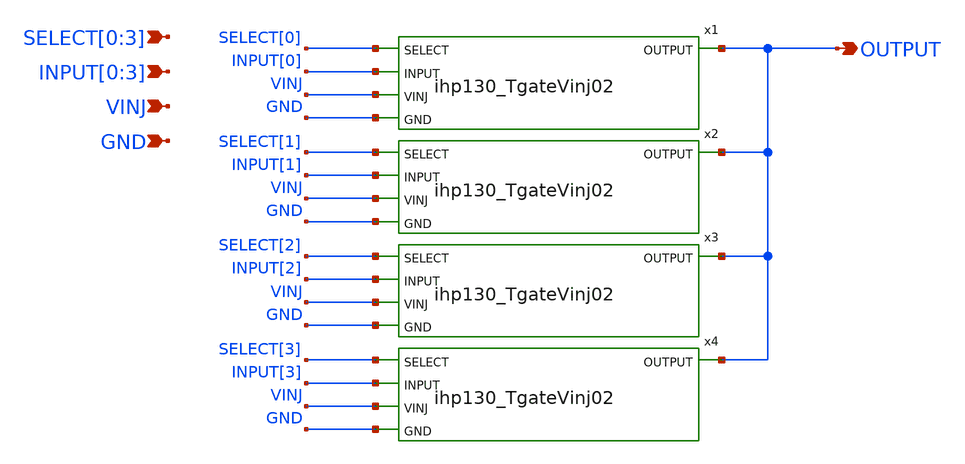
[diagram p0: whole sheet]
** sch_path: ihp130_cells/4TgateVinj/4TgateVinj.sch
**.subckt 4TgateVinj SELECT[0],SELECT[1],SELECT[2],SELECT[3] INPUT[0],INPUT[1],INPUT[2],INPUT[3]
*+ VINJ GND OUTPUT
*.ipin SELECT[0],SELECT[1],SELECT[2],SELECT[3]
*.ipin INPUT[0],INPUT[1],INPUT[2],INPUT[3]
*.ipin VINJ
*.ipin GND
*.opin OUTPUT
x1 SELECT[0] INPUT[0] VINJ GND OUTPUT ihp130_TgateVinj02
x2 SELECT[1] INPUT[1] VINJ GND OUTPUT ihp130_TgateVinj02
x3 SELECT[2] INPUT[2] VINJ GND OUTPUT ihp130_TgateVinj02
x4 SELECT[3] INPUT[3] VINJ GND OUTPUT ihp130_TgateVinj02
**.ends

* expanding   symbol:  TgateVinj02/ihp130_TgateVinj02.sym # of pins=5
** sym_path: ihp130_cells/TgateVinj02/ihp130_TgateVinj02.sym
** sch_path: ihp130_cells/TgateVinj02/ihp130_TgateVinj02.sch
.subckt ihp130_TgateVinj02 SELECT INPUT VINJ GND OUTPUT
*.ipin SELECT
*.ipin INPUT
*.ipin VINJ
*.ipin GND
*.opin OUTPUT
XM1 Selb SELECT VINJ VINJ sg13_hv_pmos w=0.42u l=0.5u ng=1 m=1 mm_ok=1
XM2 Selb SELECT GND GND sg13_hv_nmos w=0.42u l=0.5u ng=1 m=1 mm_ok=1
XM3 INPUT Selb OUTPUT VINJ sg13_hv_pmos w=0.42u l=0.5u ng=1 m=1 mm_ok=1
XM4 INPUT SELECT OUTPUT GND sg13_hv_nmos w=0.42u l=0.5u ng=1 m=1 mm_ok=1
.ends

.end
